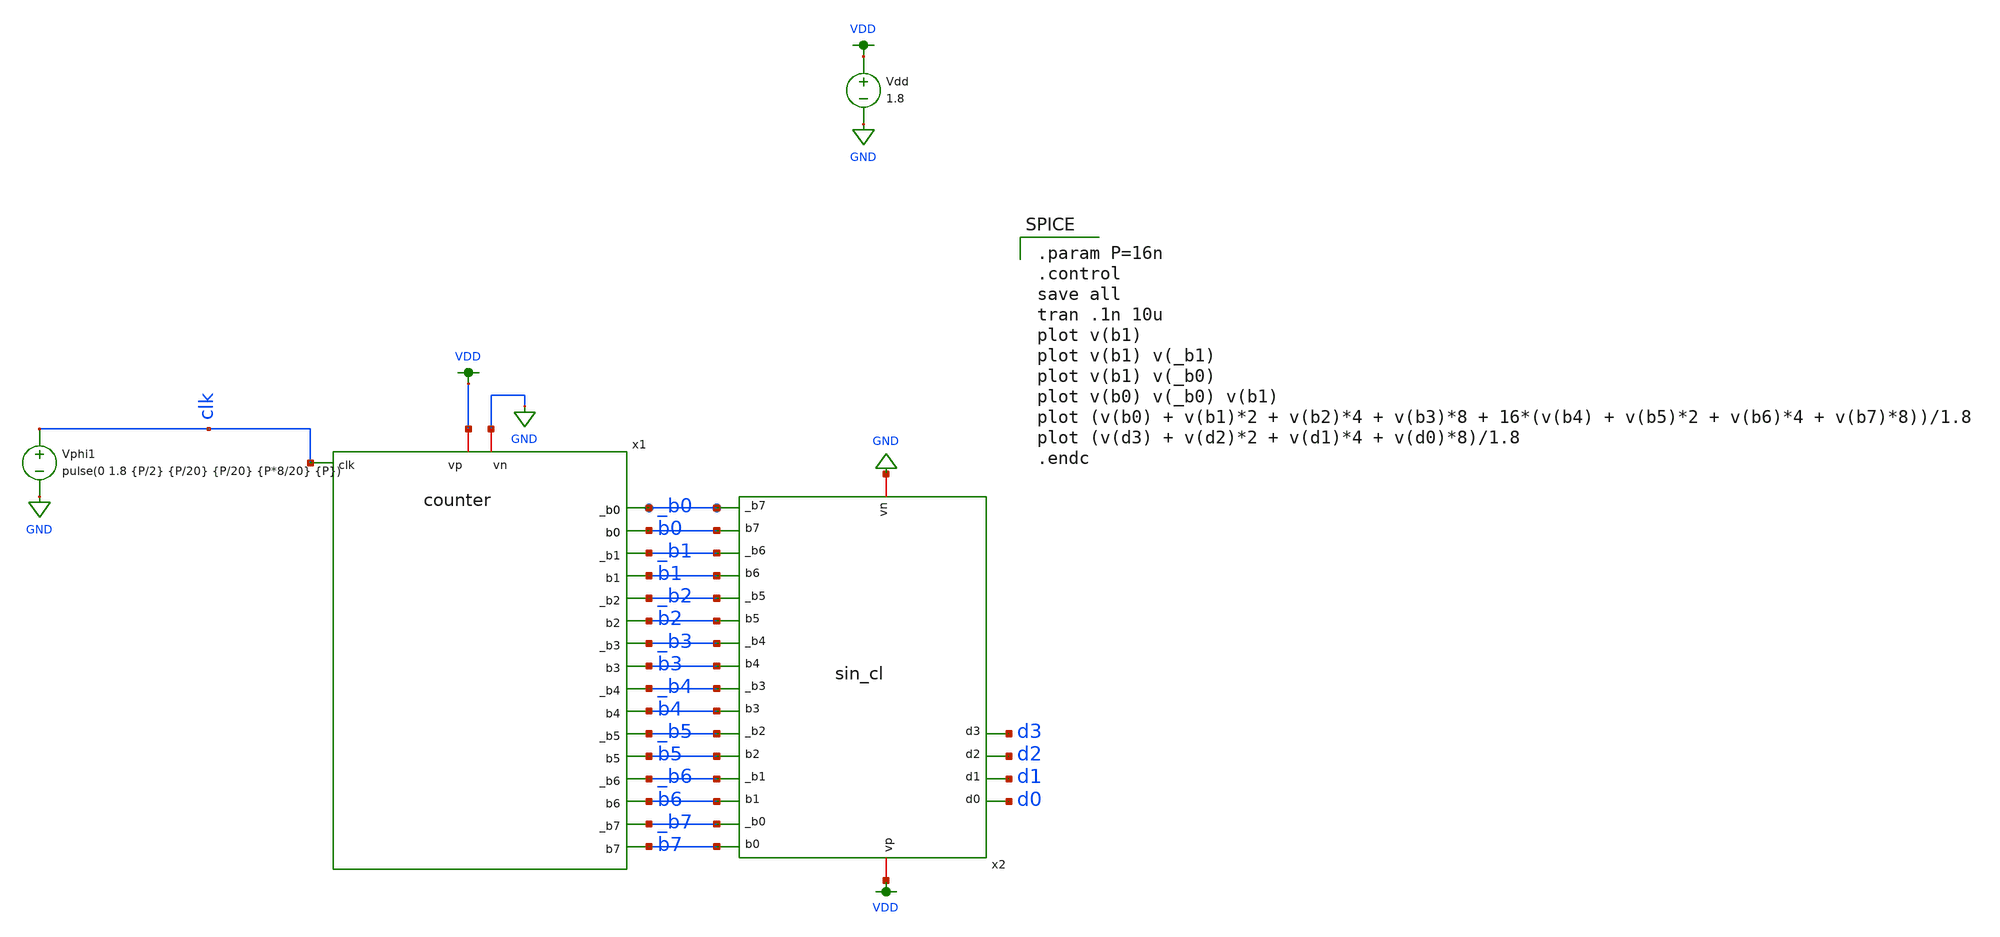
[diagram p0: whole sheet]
** sch_path: xschem/counter_testbench.sch
**.subckt counter_testbench
Vdd VDD GND 1.8
x1 VDD GND clk _b1 b1 _b2 b2 _b3 b3 _b0 b0 _b5 b5 _b6 b6 _b7 b7 _b4 b4 counter
x2 b6 _b6 b5 _b5 b4 _b4 b3 VDD _b3 GND b2 _b2 b1 _b1 d0 b7 b0 _b7 _b0 d1 d2 d3 sin_cl
Vphi1 clk GND pulse(0 1.8 {P/2} {P/20} {P/20} {P*8/20} {P})
**** begin user architecture code

.option wnflag=1
.param MC_SWITCH=0.0
.lib ~/skywater/skywater-pdk/libraries/sky130_fd_pr_ngspice/latest/models/sky130.lib.spice tt


.param P=16n
.control
save all
tran .1n 10u
plot v(b1)
plot v(b1) v(_b1)
plot v(b1) v(_b0)
plot v(b0) v(_b0) v(b1)
plot (v(b0) + v(b1)*2 + v(b2)*4 + v(b3)*8 + 16*(v(b4) + v(b5)*2 + v(b6)*4 + v(b7)*8))/1.8
plot (v(d3) + v(d2)*2 + v(d1)*4 + v(d0)*8)/1.8
.endc

**** end user architecture code
**.ends
.GLOBAL VDD
.GLOBAL GND
.end
